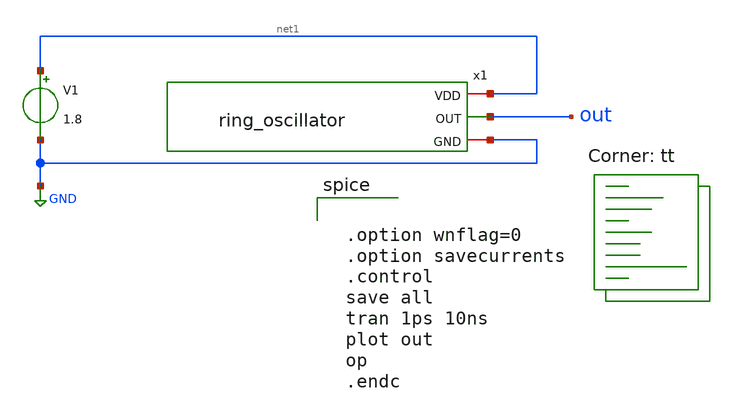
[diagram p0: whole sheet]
** sch_path: ring_oscillator_tb.sch
**.subckt ring_oscillator_tb
x1 net1 out GND ring_oscillator
V1 net1 GND 1.8
**** begin user architecture code
.lib $::SKYWATER_MODELS/sky130.lib.spice tt


 .option wnflag=0
 .option savecurrents
 .control
 save all
 tran 1ps 10ns
 plot out
 op
 .endc

**** end user architecture code
**.ends
.GLOBAL GND
.end
